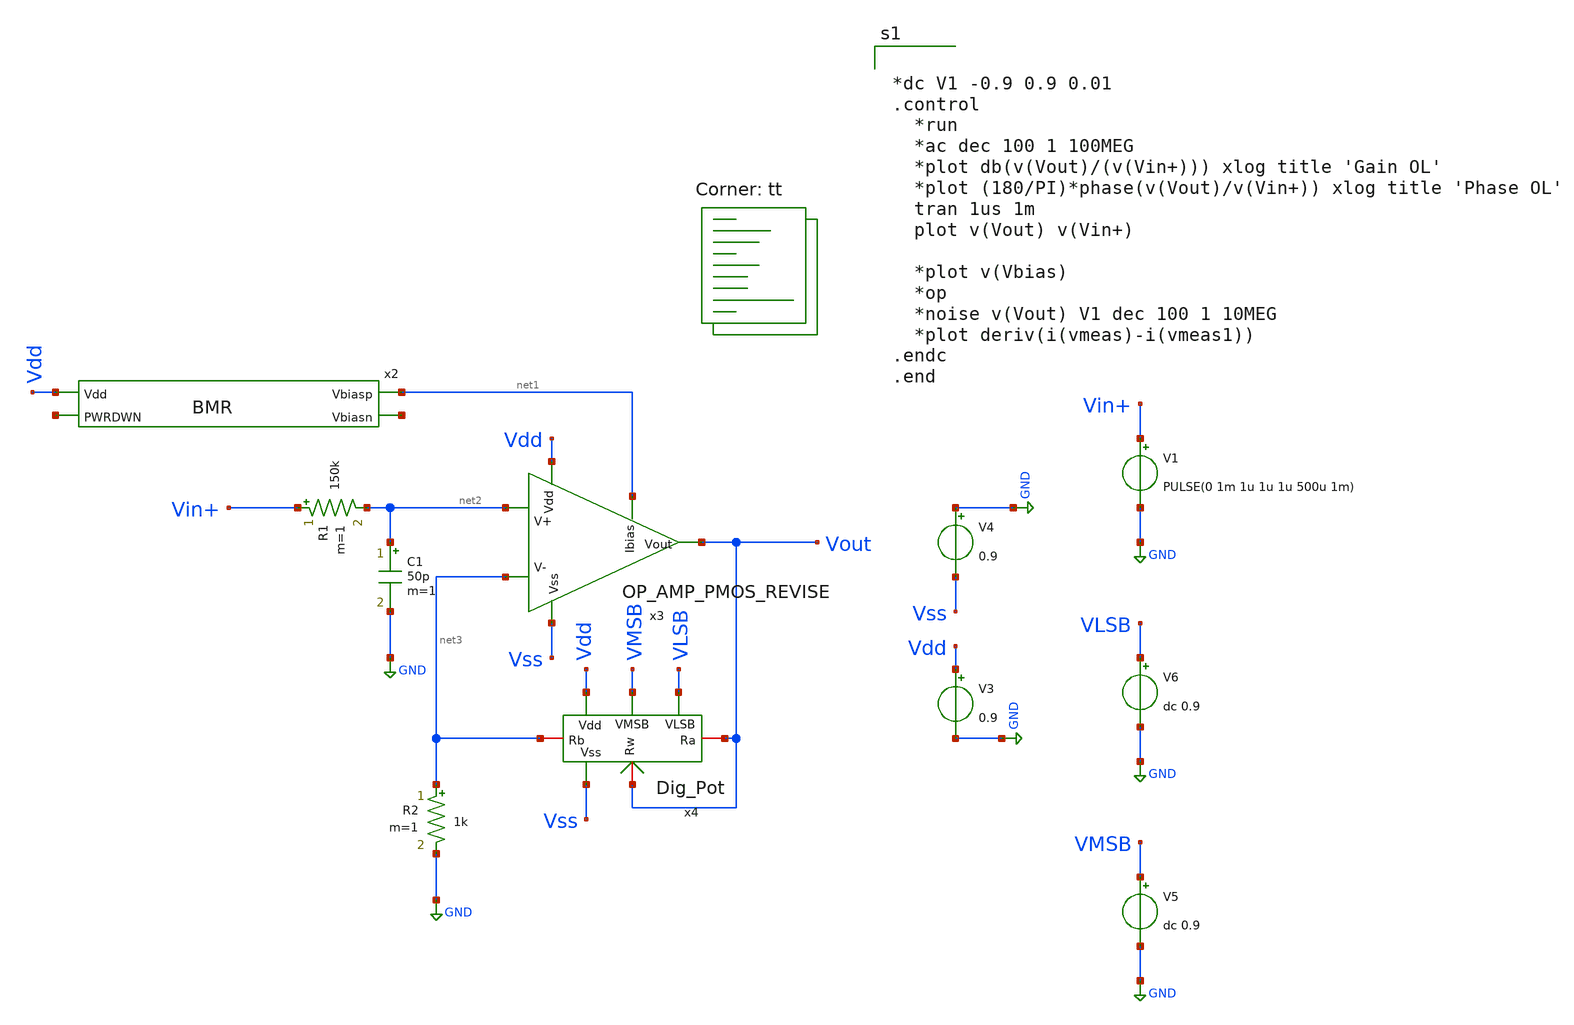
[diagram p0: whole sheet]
** sch_path: xschem/MY_LPF.sch
**.subckt MY_LPF
x2 Vdd net1 net4 net5 BMR
x3 Vdd Vss net1 Vout net2 net3 OP_AMP_PMOS_REVISE
R2 net3 GND 1k m=1
x4 Vdd Vss VLSB Vout VMSB Vout net3 Dig_Pot
R1 Vin+ net2 150k m=1
C1 net2 GND 50p m=1
V1 Vin+ GND PULSE(0 1m 1u 1u 1u 500u 1m)
V4 GND Vss 0.9
V3 Vdd GND 0.9
V5 VMSB GND dc 0.9
V6 VLSB GND dc 0.9
**** begin user architecture code
.lib $::SKYWATER_MODELS/sky130.lib.spice tt


*dc V1 -0.9 0.9 0.01
.control
  *run
  *ac dec 100 1 100MEG
  *plot db(v(Vout)/(v(Vin+))) xlog title 'Gain OL'
  *plot (180/PI)*phase(v(Vout)/v(Vin+)) xlog title 'Phase OL'
  tran 1us 1m
  plot v(Vout) v(Vin+)

  *plot v(Vbias)
  *op
  *noise v(Vout) V1 dec 100 1 10MEG
  *plot deriv(i(vmeas)-i(vmeas1))
.endc
.end

**** end user architecture code
**.ends
.GLOBAL GND
.end
